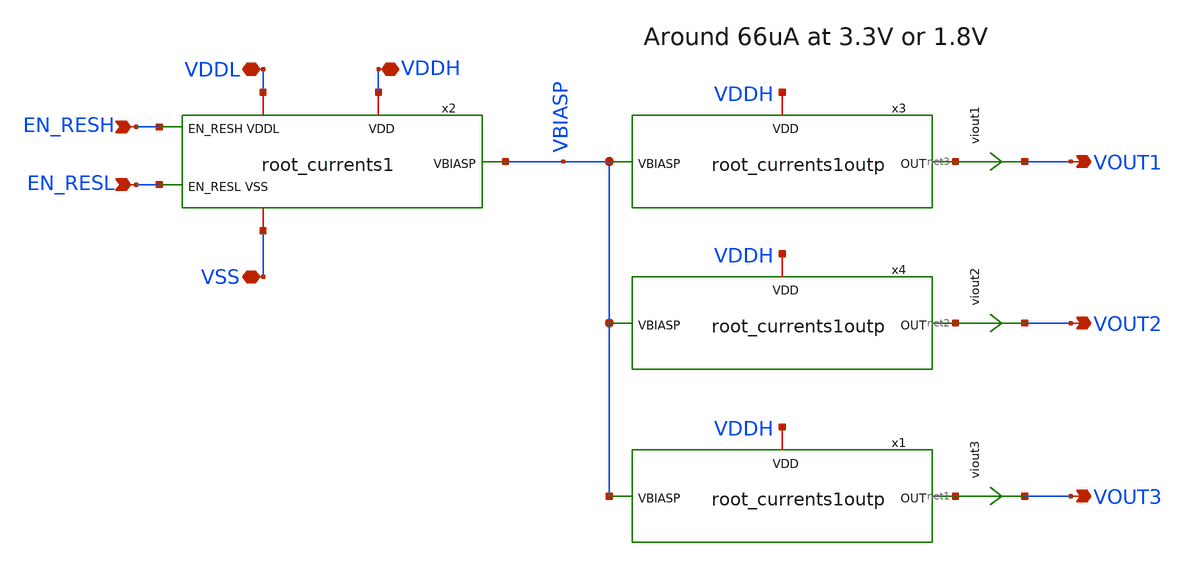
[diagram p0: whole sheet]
** sch_path: xschem/root_currents1_3outs.sch
**.subckt root_currents1_3outs EN_RESH EN_RESL VOUT1 VOUT2 VOUT3 VDDH VDDL VSS
*.ipin EN_RESH
*.ipin EN_RESL
*.opin VOUT1
*.opin VOUT2
*.opin VOUT3
*.iopin VDDH
*.iopin VDDL
*.iopin VSS
x1 VBIASP net1 VDDH root_currents1outp
viout3 net1 VOUT3 0
.save i(viout3)
x4 VBIASP net2 VDDH root_currents1outp
x2 EN_RESH EN_RESL VBIASP VDDH VDDL VSS root_currents1
viout2 net2 VOUT2 0
.save i(viout2)
viout1 net3 VOUT1 0
.save i(viout1)
x3 VBIASP net3 VDDH root_currents1outp
**.ends

* expanding   symbol:  root_currents1outp.sym # of pins=3
** sym_path: xschem/root_currents1outp.sym
** sch_path: xschem/root_currents1outp.sch
.subckt root_currents1outp VBIASP OUT VDD
*.iopin VBIASP
*.iopin OUT
*.iopin VDD
XM7 net1 VBIASP VDD VDD sky130_fd_pr__pfet_g5v0d10v5 L=0.5 W=4 nf=1 ad='int((nf+1)/2) * W/nf * 0.29'
+ as='int((nf+2)/2) * W/nf * 0.29' pd='2*int((nf+1)/2) * (W/nf + 0.29)' ps='2*int((nf+2)/2) * (W/nf + 0.29)'
+ nrd='0.29 / W' nrs='0.29 / W' sa=0 sb=0 sd=0 mult=1 m=1
viout net1 OUT 0
.save i(viout)
.ends


* expanding   symbol:  root_currents1.sym # of pins=6
** sym_path: xschem/root_currents1.sym
** sch_path: xschem/root_currents1.sch
.subckt root_currents1 EN_RESH EN_RESL VBIASP VDD VDDL VSS
*.iopin VSS
*.ipin EN_RESH
*.opin VBIASP
*.iopin VDDL
*.iopin VDD
*.ipin EN_RESL
XR1 V1 net2 net4 sky130_fd_pr__res_high_po_0p35 L=20 mult=1 m=1
XR2 V2 net3 net5 sky130_fd_pr__res_high_po_0p69 L=8 mult=1 m=1
XM4 VMID VMID VSS VSS sky130_fd_pr__nfet_01v8_lvt L=0.5 W=4 nf=1 ad='int((nf+1)/2) * W/nf * 0.29' as='int((nf+2)/2) * W/nf * 0.29'
+ pd='2*int((nf+1)/2) * (W/nf + 0.29)' ps='2*int((nf+2)/2) * (W/nf + 0.29)' nrd='0.29 / W' nrs='0.29 / W'
+ sa=0 sb=0 sd=0 mult=1 m=1
XM5 VMID VMID VSS VSS sky130_fd_pr__nfet_01v8_lvt L=0.5 W=4 nf=1 ad='int((nf+1)/2) * W/nf * 0.29' as='int((nf+2)/2) * W/nf * 0.29'
+ pd='2*int((nf+1)/2) * (W/nf + 0.29)' ps='2*int((nf+2)/2) * (W/nf + 0.29)' nrd='0.29 / W' nrs='0.29 / W'
+ sa=0 sb=0 sd=0 mult=1 m=1
XM6 net1 VMID VSS VSS sky130_fd_pr__nfet_01v8_lvt L=0.5 W=4 nf=1 ad='int((nf+1)/2) * W/nf * 0.29' as='int((nf+2)/2) * W/nf * 0.29'
+ pd='2*int((nf+1)/2) * (W/nf + 0.29)' ps='2*int((nf+2)/2) * (W/nf + 0.29)' nrd='0.29 / W' nrs='0.29 / W'
+ sa=0 sb=0 sd=0 mult=1 m=1
XM2 V1 EN_RESH_VDD VMID VSS sky130_fd_pr__nfet_g5v0d10v5 L=0.5 W=4 nf=1 ad='int((nf+1)/2) * W/nf * 0.29'
+ as='int((nf+2)/2) * W/nf * 0.29' pd='2*int((nf+1)/2) * (W/nf + 0.29)' ps='2*int((nf+2)/2) * (W/nf + 0.29)'
+ nrd='0.29 / W' nrs='0.29 / W' sa=0 sb=0 sd=0 mult=1 m=1
viout VBIASP net1 0
.save i(viout)
x1 EN_RESH EN_RESH_VDD net6 VDD VDDL VSS lvl_shift_lohi1
XM7 VBIASP VBIASP VDD VDD sky130_fd_pr__pfet_g5v0d10v5 L=0.5 W=4 nf=1 ad='int((nf+1)/2) * W/nf * 0.29'
+ as='int((nf+2)/2) * W/nf * 0.29' pd='2*int((nf+1)/2) * (W/nf + 0.29)' ps='2*int((nf+2)/2) * (W/nf + 0.29)'
+ nrd='0.29 / W' nrs='0.29 / W' sa=0 sb=0 sd=0 mult=1 m=1
vin1 VDD net2 0
.save i(vin1)
vin2 VDDL net3 0
.save i(vin2)
XM1 V2 EN_RESL VMID VSS sky130_fd_pr__nfet_01v8_lvt L=0.5 W=4 nf=1 ad='int((nf+1)/2) * W/nf * 0.29' as='int((nf+2)/2) * W/nf * 0.29'
+ pd='2*int((nf+1)/2) * (W/nf + 0.29)' ps='2*int((nf+2)/2) * (W/nf + 0.29)' nrd='0.29 / W' nrs='0.29 / W'
+ sa=0 sb=0 sd=0 mult=1 m=1
.ends


* expanding   symbol:  lvl_shift_lohi1.sym # of pins=6
** sym_path: xschem/lvl_shift_lohi1.sym
** sch_path: xschem/lvl_shift_lohi1.sch
.subckt lvl_shift_lohi1 D Q QB VDDH VDDL VSS
*.ipin D
*.opin Q
*.opin QB
*.iopin VDDH
*.iopin VDDL
*.iopin VSS
vpwr VDDL net1 0
.save i(vpwr)
XM1 QB Q VDDH VDDH sky130_fd_pr__pfet_g5v0d10v5 L=0.5 W=2 nf=1 ad='int((nf+1)/2) * W/nf * 0.29' as='int((nf+2)/2) * W/nf * 0.29'
+ pd='2*int((nf+1)/2) * (W/nf + 0.29)' ps='2*int((nf+2)/2) * (W/nf + 0.29)' nrd='0.29 / W' nrs='0.29 / W'
+ sa=0 sb=0 sd=0 mult=1 m=1
XM2 Q QB VDDH VDDH sky130_fd_pr__pfet_g5v0d10v5 L=0.5 W=2 nf=1 ad='int((nf+1)/2) * W/nf * 0.29' as='int((nf+2)/2) * W/nf * 0.29'
+ pd='2*int((nf+1)/2) * (W/nf + 0.29)' ps='2*int((nf+2)/2) * (W/nf + 0.29)' nrd='0.29 / W' nrs='0.29 / W'
+ sa=0 sb=0 sd=0 mult=1 m=1
XM3 QB D VSS VSS sky130_fd_pr__nfet_g5v0d10v5 L=0.5 W=4 nf=1 ad='int((nf+1)/2) * W/nf * 0.29' as='int((nf+2)/2) * W/nf * 0.29'
+ pd='2*int((nf+1)/2) * (W/nf + 0.29)' ps='2*int((nf+2)/2) * (W/nf + 0.29)' nrd='0.29 / W' nrs='0.29 / W'
+ sa=0 sb=0 sd=0 mult=1 m=1
XM4 Q DB VSS VSS sky130_fd_pr__nfet_g5v0d10v5 L=0.5 W=4 nf=1 ad='int((nf+1)/2) * W/nf * 0.29' as='int((nf+2)/2) * W/nf * 0.29'
+ pd='2*int((nf+1)/2) * (W/nf + 0.29)' ps='2*int((nf+2)/2) * (W/nf + 0.29)' nrd='0.29 / W' nrs='0.29 / W'
+ sa=0 sb=0 sd=0 mult=1 m=1
XM5 DB D VSS VSS sky130_fd_pr__nfet_01v8_lvt L=0.5 W=1 nf=1 ad='int((nf+1)/2) * W/nf * 0.29' as='int((nf+2)/2) * W/nf * 0.29'
+ pd='2*int((nf+1)/2) * (W/nf + 0.29)' ps='2*int((nf+2)/2) * (W/nf + 0.29)' nrd='0.29 / W' nrs='0.29 / W'
+ sa=0 sb=0 sd=0 mult=1 m=1
XM6 DB D net1 VDDL sky130_fd_pr__pfet_01v8_lvt L=0.5 W=2 nf=1 ad='int((nf+1)/2) * W/nf * 0.29' as='int((nf+2)/2) * W/nf * 0.29'
+ pd='2*int((nf+1)/2) * (W/nf + 0.29)' ps='2*int((nf+2)/2) * (W/nf + 0.29)' nrd='0.29 / W' nrs='0.29 / W'
+ sa=0 sb=0 sd=0 mult=1 m=1
.ends

.end
